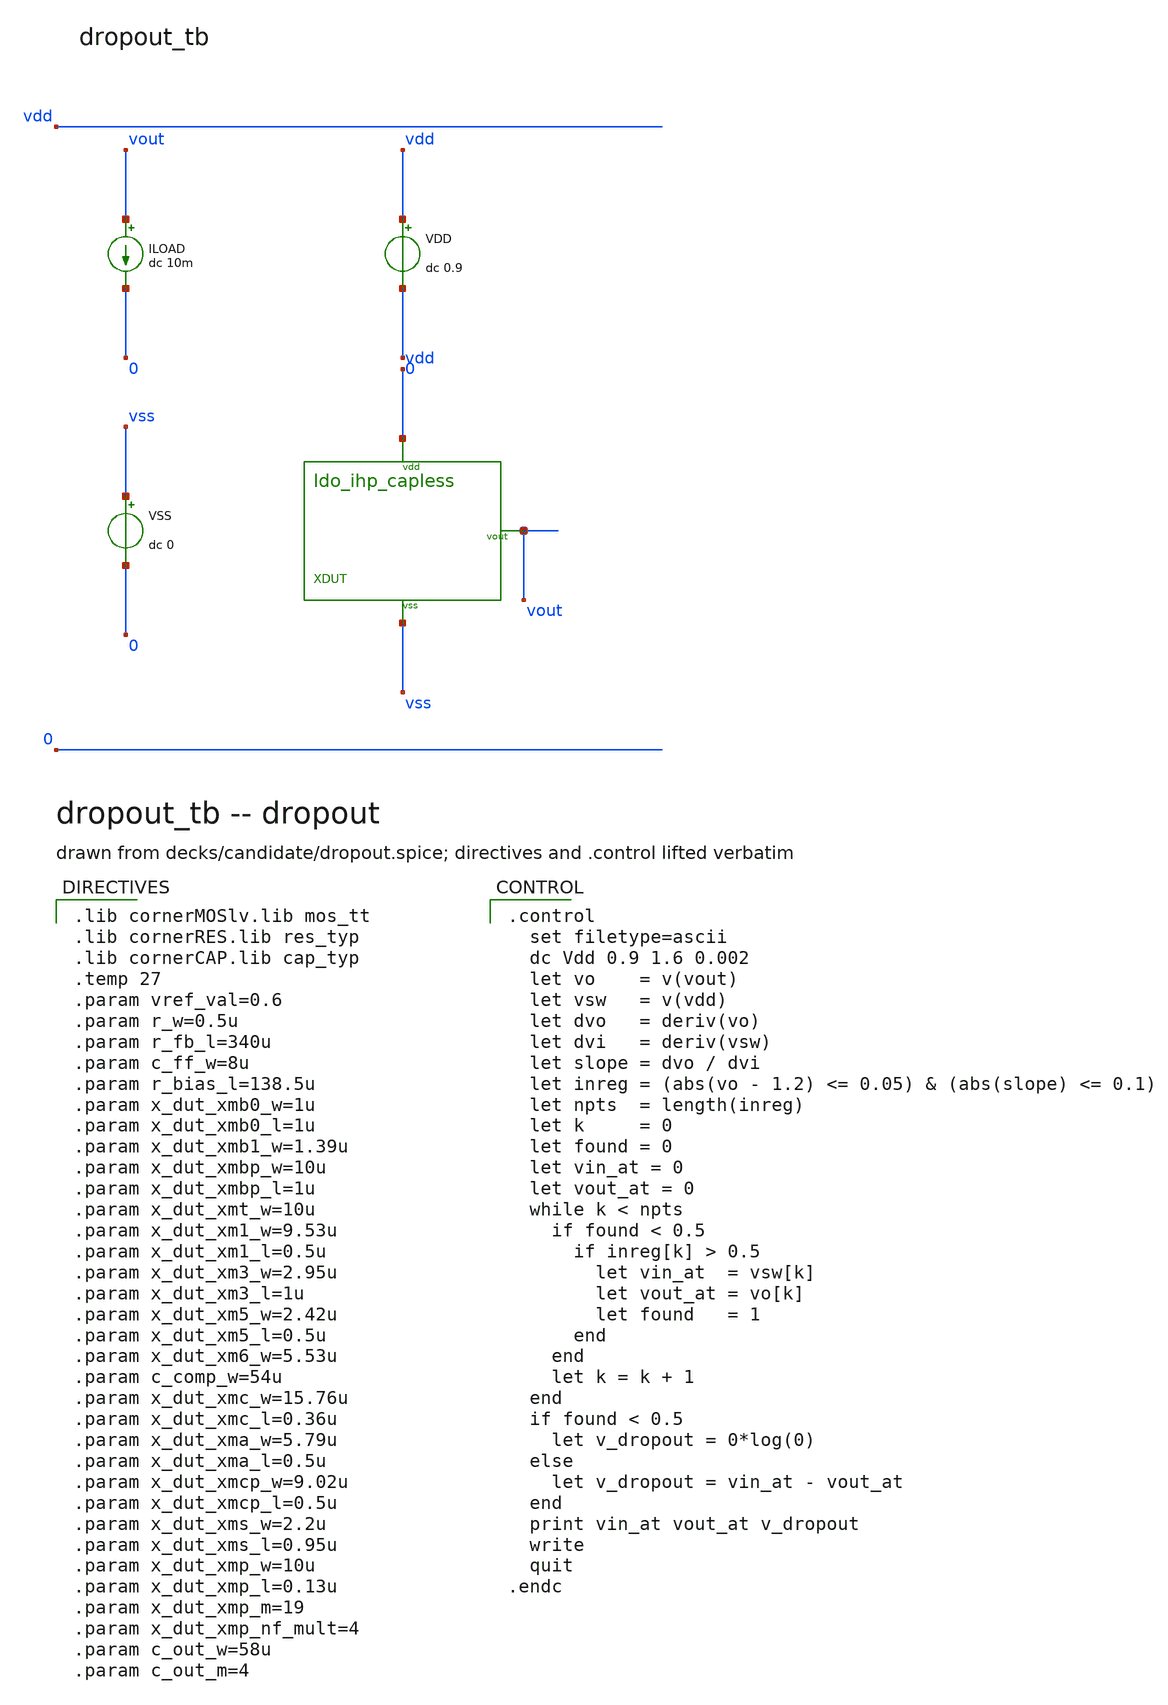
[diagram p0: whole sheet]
** sch_path: analog-db/circuits/ldo_010_capless_lowiq/pdk/ihp-sg13g2/schematic/benches/dropout_tb.sch
**.subckt dropout_tb
VDD vdd 0 dc 0.9
VSS vss 0 dc 0
ILOAD vout 0 dc 10m
XDUT vdd vout vss ldo_ihp_capless
**** begin user architecture code

.lib cornerMOSlv.lib mos_tt
.lib cornerRES.lib res_typ
.lib cornerCAP.lib cap_typ
.temp 27
.param vref_val=0.6
.param r_w=0.5u
.param r_fb_l=340u
.param c_ff_w=8u
.param r_bias_l=138.5u
.param x_dut_xmb0_w=1u
.param x_dut_xmb0_l=1u
.param x_dut_xmb1_w=1.39u
.param x_dut_xmbp_w=10u
.param x_dut_xmbp_l=1u
.param x_dut_xmt_w=10u
.param x_dut_xm1_w=9.53u
.param x_dut_xm1_l=0.5u
.param x_dut_xm3_w=2.95u
.param x_dut_xm3_l=1u
.param x_dut_xm5_w=2.42u
.param x_dut_xm5_l=0.5u
.param x_dut_xm6_w=5.53u
.param c_comp_w=54u
.param x_dut_xmc_w=15.76u
.param x_dut_xmc_l=0.36u
.param x_dut_xma_w=5.79u
.param x_dut_xma_l=0.5u
.param x_dut_xmcp_w=9.02u
.param x_dut_xmcp_l=0.5u
.param x_dut_xms_w=2.2u
.param x_dut_xms_l=0.95u
.param x_dut_xmp_w=10u
.param x_dut_xmp_l=0.13u
.param x_dut_xmp_m=19
.param x_dut_xmp_nf_mult=4
.param c_out_w=58u
.param c_out_m=4


.control
  set filetype=ascii
  dc Vdd 0.9 1.6 0.002
  let vo    = v(vout)
  let vsw   = v(vdd)
  let dvo   = deriv(vo)
  let dvi   = deriv(vsw)
  let slope = dvo / dvi
  let inreg = (abs(vo - 1.2) <= 0.05) & (abs(slope) <= 0.1)
  let npts  = length(inreg)
  let k     = 0
  let found = 0
  let vin_at = 0
  let vout_at = 0
  while k < npts
    if found < 0.5
      if inreg[k] > 0.5
        let vin_at  = vsw[k]
        let vout_at = vo[k]
        let found   = 1
      end
    end
    let k = k + 1
  end
  if found < 0.5
    let v_dropout = 0*log(0)
  else
    let v_dropout = vin_at - vout_at
  end
  print vin_at vout_at v_dropout
  write
  quit
.endc

**** end user architecture code
**.ends

* expanding   symbol:  ldo_ihp_capless.sym # of pins=3
** sym_path: analog-db/circuits/ldo_010_capless_lowiq/pdk/ihp-sg13g2/schematic/ldo_ihp_capless.sym
** sch_path: analog-db/circuits/ldo_010_capless_lowiq/pdk/ihp-sg13g2/schematic/ldo_ihp_capless.sch
.subckt ldo_ihp_capless vdd vout vss
*.iopin vdd
*.opin vout
*.iopin vss
xbias_ref nbias pbias vdd vss bias_ref
xea_stage1 fb pbias vref ea_o1 vdd vss ea_stage1
xea_stage2 pbias ea_o1 ea_out vdd vss ea_stage2
xfvf_output ea_out nbias vout vdd vss fvf_output
xfb_divider fb lp_brk vss fb_divider
VREF vref vss dc {vref_val}
VLP lp_brk vout dc 0
XCOUT vout vss cap_cmim w=c_out_w l=c_out_w m=c_out_m
.ends


* expanding   symbol:  blocks/bias_ref.sym # of pins=4
** sym_path: analog-db/circuits/ldo_010_capless_lowiq/pdk/ihp-sg13g2/schematic/blocks/bias_ref.sym
** sch_path: analog-db/circuits/ldo_010_capless_lowiq/pdk/ihp-sg13g2/schematic/blocks/bias_ref.sch
.subckt bias_ref nbias pbias vdd vss
*.opin nbias
*.opin pbias
*.iopin vdd
*.iopin vss
XRB_1 vdd n_rb_1 vss rhigh w=r_w l={r_bias_l/5} m=1 b=0
XRB_2 n_rb_1 n_rb_2 vss rhigh w=r_w l={r_bias_l/5} m=1 b=0
XRB_3 n_rb_2 n_rb_3 vss rhigh w=r_w l={r_bias_l/5} m=1 b=0
XRB_4 n_rb_3 n_rb_4 vss rhigh w=r_w l={r_bias_l/5} m=1 b=0
XRB_5 n_rb_4 nbias vss rhigh w=r_w l={r_bias_l/5} m=1 b=0
XMB0A nbias nbias vss vss sg13_lv_nmos w={x_dut_xmb0_w/2} l=x_dut_xmb0_l ng=1 m=1 mm_ok=1
XMB0B nbias nbias vss vss sg13_lv_nmos w={x_dut_xmb0_w/2} l=x_dut_xmb0_l ng=1 m=1 mm_ok=1
XMB1A pbias nbias vss vss sg13_lv_nmos w={x_dut_xmb1_w/2} l=x_dut_xmb0_l ng=1 m=1 mm_ok=1
XMB1B pbias nbias vss vss sg13_lv_nmos w={x_dut_xmb1_w/2} l=x_dut_xmb0_l ng=1 m=1 mm_ok=1
XMBP pbias pbias vdd vdd sg13_lv_pmos w=x_dut_xmbp_w l=x_dut_xmbp_l ng=1 m=1 mm_ok=1
.ends


* expanding   symbol:  blocks/ea_stage1.sym # of pins=6
** sym_path: analog-db/circuits/ldo_010_capless_lowiq/pdk/ihp-sg13g2/schematic/blocks/ea_stage1.sym
** sch_path: analog-db/circuits/ldo_010_capless_lowiq/pdk/ihp-sg13g2/schematic/blocks/ea_stage1.sch
.subckt ea_stage1 fb pbias vref ea_o1 vdd vss
*.ipin fb
*.ipin pbias
*.ipin vref
*.opin ea_o1
*.iopin vdd
*.iopin vss
XMT ea_tail pbias vdd vdd sg13_lv_pmos w=x_dut_xmt_w l=x_dut_xmbp_l ng=1 m=1 mm_ok=1
XM1A ea_n fb ea_tail vdd sg13_lv_pmos w={x_dut_xm1_w/2} l=x_dut_xm1_l ng=1 m=1 mm_ok=1
XM1B ea_n fb ea_tail vdd sg13_lv_pmos w={x_dut_xm1_w/2} l=x_dut_xm1_l ng=1 m=1 mm_ok=1
XM2A ea_o1 vref ea_tail vdd sg13_lv_pmos w={x_dut_xm1_w/2} l=x_dut_xm1_l ng=1 m=1 mm_ok=1
XM2B ea_o1 vref ea_tail vdd sg13_lv_pmos w={x_dut_xm1_w/2} l=x_dut_xm1_l ng=1 m=1 mm_ok=1
XM3A ea_n ea_n vss vss sg13_lv_nmos w={x_dut_xm3_w/2} l=x_dut_xm3_l ng=1 m=1 mm_ok=1
XM3B ea_n ea_n vss vss sg13_lv_nmos w={x_dut_xm3_w/2} l=x_dut_xm3_l ng=1 m=1 mm_ok=1
XM4A ea_o1 ea_n vss vss sg13_lv_nmos w={x_dut_xm3_w/2} l=x_dut_xm3_l ng=1 m=1 mm_ok=1
XM4B ea_o1 ea_n vss vss sg13_lv_nmos w={x_dut_xm3_w/2} l=x_dut_xm3_l ng=1 m=1 mm_ok=1
.ends


* expanding   symbol:  blocks/ea_stage2.sym # of pins=5
** sym_path: analog-db/circuits/ldo_010_capless_lowiq/pdk/ihp-sg13g2/schematic/blocks/ea_stage2.sym
** sch_path: analog-db/circuits/ldo_010_capless_lowiq/pdk/ihp-sg13g2/schematic/blocks/ea_stage2.sch
.subckt ea_stage2 pbias ea_o1 ea_out vdd vss
*.ipin pbias
*.iopin vdd
*.iopin ea_o1
*.iopin vss
*.opin ea_out
XM5 ea_out ea_o1 vss vss sg13_lv_nmos w=x_dut_xm5_w l=x_dut_xm5_l ng=1 m=1 mm_ok=1
XM6 ea_out pbias vdd vdd sg13_lv_pmos w=x_dut_xm6_w l=x_dut_xmbp_l ng=1 m=1 mm_ok=1
XCC ea_out ea_o1 cap_cmim w=c_comp_w l=c_comp_w m=1
.ends


* expanding   symbol:  blocks/fvf_output.sym # of pins=5
** sym_path: analog-db/circuits/ldo_010_capless_lowiq/pdk/ihp-sg13g2/schematic/blocks/fvf_output.sym
** sch_path: analog-db/circuits/ldo_010_capless_lowiq/pdk/ihp-sg13g2/schematic/blocks/fvf_output.sch
.subckt fvf_output ea_out nbias vout vdd vss
*.ipin nbias
*.ipin ea_out
*.iopin vdd
*.iopin vss
*.opin vout
XMC x1 ea_out vout vdd sg13_lv_pmos w=x_dut_xmc_w l=x_dut_xmc_l ng=1 m=1 mm_ok=1
XMA x1 x1 vss vss sg13_lv_nmos w=x_dut_xma_w l=x_dut_xma_l ng=1 m=1 mm_ok=1
XMB y x1 vss vss sg13_lv_nmos w=x_dut_xma_w l=x_dut_xma_l ng=1 m=1 mm_ok=1
XMCP y y vdd vdd sg13_lv_pmos w=x_dut_xmcp_w l=x_dut_xmcp_l ng=1 m=1 mm_ok=1
XMD gate y vdd vdd sg13_lv_pmos w=x_dut_xmcp_w l=x_dut_xmcp_l ng=1 m=1 mm_ok=1
XMSA gate nbias vss vss sg13_lv_nmos w={x_dut_xms_w/2} l=x_dut_xms_l ng=1 m=1 mm_ok=1
XMSB gate nbias vss vss sg13_lv_nmos w={x_dut_xms_w/2} l=x_dut_xms_l ng=1 m=1 mm_ok=1
XMP vout gate vdd vdd sg13_lv_pmos w={x_dut_xmp_w/x_dut_xmp_nf_mult} l=x_dut_xmp_l ng=1 m={x_dut_xmp_m*x_dut_xmp_nf_mult}
+ mm_ok=1
.ends


* expanding   symbol:  blocks/fb_divider.sym # of pins=3
** sym_path: analog-db/circuits/ldo_010_capless_lowiq/pdk/ihp-sg13g2/schematic/blocks/fb_divider.sym
** sch_path: analog-db/circuits/ldo_010_capless_lowiq/pdk/ihp-sg13g2/schematic/blocks/fb_divider.sch
.subckt fb_divider fb lp_brk vss
*.iopin lp_brk
*.iopin fb
*.iopin vss
XR1_1 lp_brk n_r1_1 vss rhigh w=r_w l={r_fb_l/8} m=1 b=0
XR1_2 n_r1_1 n_r1_2 vss rhigh w=r_w l={r_fb_l/8} m=1 b=0
XR1_3 n_r1_2 n_r1_3 vss rhigh w=r_w l={r_fb_l/8} m=1 b=0
XR1_4 n_r1_3 n_r1_4 vss rhigh w=r_w l={r_fb_l/8} m=1 b=0
XR1_5 n_r1_4 n_r1_5 vss rhigh w=r_w l={r_fb_l/8} m=1 b=0
XR1_6 n_r1_5 n_r1_6 vss rhigh w=r_w l={r_fb_l/8} m=1 b=0
XR1_7 n_r1_6 n_r1_7 vss rhigh w=r_w l={r_fb_l/8} m=1 b=0
XR1_8 n_r1_7 fb vss rhigh w=r_w l={r_fb_l/8} m=1 b=0
XR2_1 fb n_r2_1 vss rhigh w=r_w l={r_fb_l/8} m=1 b=0
XR2_2 n_r2_1 n_r2_2 vss rhigh w=r_w l={r_fb_l/8} m=1 b=0
XR2_3 n_r2_2 n_r2_3 vss rhigh w=r_w l={r_fb_l/8} m=1 b=0
XR2_4 n_r2_3 n_r2_4 vss rhigh w=r_w l={r_fb_l/8} m=1 b=0
XR2_5 n_r2_4 n_r2_5 vss rhigh w=r_w l={r_fb_l/8} m=1 b=0
XR2_6 n_r2_5 n_r2_6 vss rhigh w=r_w l={r_fb_l/8} m=1 b=0
XR2_7 n_r2_6 n_r2_7 vss rhigh w=r_w l={r_fb_l/8} m=1 b=0
XR2_8 n_r2_7 vss vss rhigh w=r_w l={r_fb_l/8} m=1 b=0
XCFF lp_brk fb cap_cmim w=c_ff_w l=c_ff_w m=1
.ends

.end
